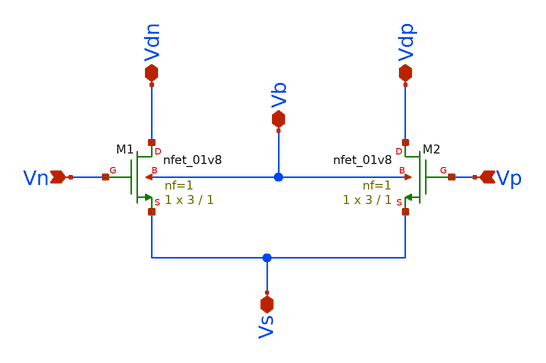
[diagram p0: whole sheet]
** sch_path: Circuits/DiffAmp/DiffPair.sch
**.subckt DiffPair Vn Vp Vb Vs Vdn Vdp
*.ipin Vn
*.ipin Vp
*.iopin Vb
*.iopin Vs
*.iopin Vdn
*.iopin Vdp
XM1 Vdn Vn Vs Vb sky130_fd_pr__nfet_01v8 L=1 W=3 nf=1 ad='int((nf+1)/2) * W/nf * 0.29' as='int((nf+2)/2) * W/nf * 0.29'
+ pd='2*int((nf+1)/2) * (W/nf + 0.29)' ps='2*int((nf+2)/2) * (W/nf + 0.29)' nrd='0.29 / W' nrs='0.29 / W'
+ sa=0 sb=0 sd=0 mult=1 m=1
XM2 Vdp Vp Vs Vb sky130_fd_pr__nfet_01v8 L=1 W=3 nf=1 ad='int((nf+1)/2) * W/nf * 0.29' as='int((nf+2)/2) * W/nf * 0.29'
+ pd='2*int((nf+1)/2) * (W/nf + 0.29)' ps='2*int((nf+2)/2) * (W/nf + 0.29)' nrd='0.29 / W' nrs='0.29 / W'
+ sa=0 sb=0 sd=0 mult=1 m=1
**.ends
.end
